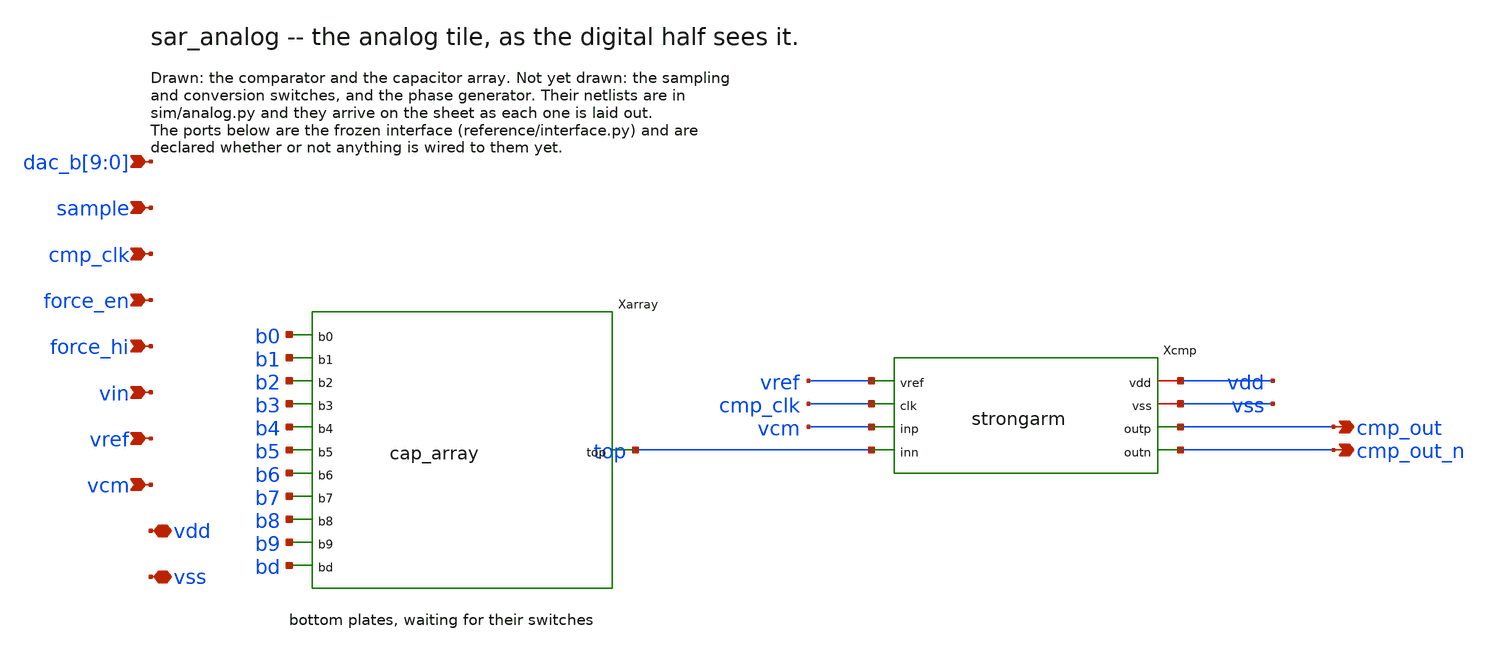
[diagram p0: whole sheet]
** sch_path: xschem/sar_analog.sch
**.subckt sar_analog
*+ dac_b[9],dac_b[8],dac_b[7],dac_b[6],dac_b[5],dac_b[4],dac_b[3],dac_b[2],dac_b[1],dac_b[0] sample cmp_clk force_en force_hi vin vref vcm vdd vss cmp_out cmp_out_n
*.ipin dac_b[9],dac_b[8],dac_b[7],dac_b[6],dac_b[5],dac_b[4],dac_b[3],dac_b[2],dac_b[1],dac_b[0]
*.ipin sample
*.ipin cmp_clk
*.ipin force_en
*.ipin force_hi
*.ipin vin
*.ipin vref
*.ipin vcm
*.iopin vdd
*.iopin vss
*.opin cmp_out
*.opin cmp_out_n
Xcmp vdd vss vref cmp_clk vcm top cmp_out cmp_out_n strongarm
Xarray top b0 b1 b2 b3 b4 b5 b6 b7 b8 b9 bd cap_array
**.ends

* expanding   symbol:  strongarm.sym # of pins=8
** sym_path: xschem/strongarm.sym
** sch_path: xschem/strongarm.sch
.subckt strongarm vdd vss vref clk inp inn outp outn
*.iopin vdd
*.iopin vss
*.ipin vref
*.ipin clk
*.ipin inp
*.ipin inn
*.opin outp
*.opin outn
Xinvp clk_i clk vdd vdd sky130_fd_pr__pfet_01v8 L=0.15 W=2 nf=1 ad='int((nf+1)/2) * W/nf * 0.29' as='int((nf+2)/2) * W/nf * 0.29'
+ pd='2*int((nf+1)/2) * (W/nf + 0.29)' ps='2*int((nf+2)/2) * (W/nf + 0.29)' nrd='0.29 / W' nrs='0.29 / W'
+ sa=0 sb=0 sd=0 mult=1 m=1
Xinvn clk_i clk vss vss sky130_fd_pr__nfet_01v8 L=0.15 W=2 nf=1 ad='int((1 + 1)/2) * 2 / 1 * 0.29' as='int((1 + 2)/2) * 2 / 1 * 0.29'
+ pd='2*int((1 + 1)/2) * (2 / 1 + 0.29)' ps='2*int((1 + 2)/2) * (2 / 1 + 0.29)' nrd='0.29 / 2 ' nrs='0.29 / 2 '
+ sa=0 sb=0 sd=0 mult=1 m=1
Xbref bias vref vss vss sky130_fd_pr__nfet_01v8 L=2 W=1 nf=1 ad='int((1 + 1)/2) * 1 / 1 * 0.29' as='int((1 + 2)/2) * 1 / 1 * 0.29'
+ pd='2*int((1 + 1)/2) * (1 / 1 + 0.29)' ps='2*int((1 + 2)/2) * (1 / 1 + 0.29)' nrd='0.29 / 1 ' nrs='0.29 / 1 '
+ sa=0 sb=0 sd=0 mult=1 m=1
Xbdio bias bias vdd vdd sky130_fd_pr__pfet_01v8 L=0.5 W=1 nf=1 ad='int((nf+1)/2) * W/nf * 0.29' as='int((nf+2)/2) * W/nf * 0.29'
+ pd='2*int((nf+1)/2) * (W/nf + 0.29)' ps='2*int((nf+2)/2) * (W/nf + 0.29)' nrd='0.29 / W' nrs='0.29 / W'
+ sa=0 sb=0 sd=0 mult=1 m=1
Xbgoff tgate clk vdd vdd sky130_fd_pr__pfet_01v8 L=0.15 W=1 nf=1 ad='int((nf+1)/2) * W/nf * 0.29' as='int((nf+2)/2) * W/nf * 0.29'
+ pd='2*int((nf+1)/2) * (W/nf + 0.29)' ps='2*int((nf+2)/2) * (W/nf + 0.29)' nrd='0.29 / W' nrs='0.29 / W'
+ sa=0 sb=0 sd=0 mult=1 m=1
Xbgon bias clk tgate vss sky130_fd_pr__nfet_01v8 L=0.15 W=1 nf=1 ad='int((1 + 1)/2) * 1 / 1 * 0.29' as='int((1 + 2)/2) * 1 / 1 * 0.29'
+ pd='2*int((1 + 1)/2) * (1 / 1 + 0.29)' ps='2*int((1 + 2)/2) * (1 / 1 + 0.29)' nrd='0.29 / 1 ' nrs='0.29 / 1 '
+ sa=0 sb=0 sd=0 mult=1 m=1
Cbias bias vss 1e-13 m=1
Xtail tail tgate vdd vdd sky130_fd_pr__pfet_01v8 L=0.5 W=2 nf=1 ad='int((nf+1)/2) * W/nf * 0.29' as='int((nf+2)/2) * W/nf * 0.29'
+ pd='2*int((nf+1)/2) * (W/nf + 0.29)' ps='2*int((nf+2)/2) * (W/nf + 0.29)' nrd='0.29 / W' nrs='0.29 / W'
+ sa=0 sb=0 sd=0 mult=1 m=1
Xinp xn inp tail vdd sky130_fd_pr__pfet_01v8 L=0.5 W=4 nf=1 ad='int((nf+1)/2) * W/nf * 0.29' as='int((nf+2)/2) * W/nf * 0.29'
+ pd='2*int((nf+1)/2) * (W/nf + 0.29)' ps='2*int((nf+2)/2) * (W/nf + 0.29)' nrd='0.29 / W' nrs='0.29 / W'
+ sa=0 sb=0 sd=0 mult=1 m=1
Xinn xp inn tail vdd sky130_fd_pr__pfet_01v8 L=0.5 W=4 nf=1 ad='int((nf+1)/2) * W/nf * 0.29' as='int((nf+2)/2) * W/nf * 0.29'
+ pd='2*int((nf+1)/2) * (W/nf + 0.29)' ps='2*int((nf+2)/2) * (W/nf + 0.29)' nrd='0.29 / W' nrs='0.29 / W'
+ sa=0 sb=0 sd=0 mult=1 m=1
Xlchp outp outn xp vdd sky130_fd_pr__pfet_01v8 L=0.15 W=1 nf=1 ad='int((nf+1)/2) * W/nf * 0.29' as='int((nf+2)/2) * W/nf * 0.29'
+ pd='2*int((nf+1)/2) * (W/nf + 0.29)' ps='2*int((nf+2)/2) * (W/nf + 0.29)' nrd='0.29 / W' nrs='0.29 / W'
+ sa=0 sb=0 sd=0 mult=1 m=1
Xlchn outn outp xn vdd sky130_fd_pr__pfet_01v8 L=0.15 W=1 nf=1 ad='int((nf+1)/2) * W/nf * 0.29' as='int((nf+2)/2) * W/nf * 0.29'
+ pd='2*int((nf+1)/2) * (W/nf + 0.29)' ps='2*int((nf+2)/2) * (W/nf + 0.29)' nrd='0.29 / W' nrs='0.29 / W'
+ sa=0 sb=0 sd=0 mult=1 m=1
Xldp outp outn vss vss sky130_fd_pr__nfet_01v8 L=0.15 W=2 nf=1 ad='int((1 + 1)/2) * 2 / 1 * 0.29' as='int((1 + 2)/2) * 2 / 1 * 0.29'
+ pd='2*int((1 + 1)/2) * (2 / 1 + 0.29)' ps='2*int((1 + 2)/2) * (2 / 1 + 0.29)' nrd='0.29 / 2 ' nrs='0.29 / 2 '
+ sa=0 sb=0 sd=0 mult=1 m=1
Xldn outn outp vss vss sky130_fd_pr__nfet_01v8 L=0.15 W=2 nf=1 ad='int((1 + 1)/2) * 2 / 1 * 0.29' as='int((1 + 2)/2) * 2 / 1 * 0.29'
+ pd='2*int((1 + 1)/2) * (2 / 1 + 0.29)' ps='2*int((1 + 2)/2) * (2 / 1 + 0.29)' nrd='0.29 / 2 ' nrs='0.29 / 2 '
+ sa=0 sb=0 sd=0 mult=1 m=1
Xprep outp clk_i vss vss sky130_fd_pr__nfet_01v8 L=0.15 W=2 nf=1 ad='int((1 + 1)/2) * 2 / 1 * 0.29' as='int((1 + 2)/2) * 2 / 1 * 0.29'
+ pd='2*int((1 + 1)/2) * (2 / 1 + 0.29)' ps='2*int((1 + 2)/2) * (2 / 1 + 0.29)' nrd='0.29 / 2 ' nrs='0.29 / 2 '
+ sa=0 sb=0 sd=0 mult=1 m=1
Xpren outn clk_i vss vss sky130_fd_pr__nfet_01v8 L=0.15 W=2 nf=1 ad='int((1 + 1)/2) * 2 / 1 * 0.29' as='int((1 + 2)/2) * 2 / 1 * 0.29'
+ pd='2*int((1 + 1)/2) * (2 / 1 + 0.29)' ps='2*int((1 + 2)/2) * (2 / 1 + 0.29)' nrd='0.29 / 2 ' nrs='0.29 / 2 '
+ sa=0 sb=0 sd=0 mult=1 m=1
Xprxp xp clk_i vss vss sky130_fd_pr__nfet_01v8 L=0.15 W=2 nf=1 ad='int((1 + 1)/2) * 2 / 1 * 0.29' as='int((1 + 2)/2) * 2 / 1 * 0.29'
+ pd='2*int((1 + 1)/2) * (2 / 1 + 0.29)' ps='2*int((1 + 2)/2) * (2 / 1 + 0.29)' nrd='0.29 / 2 ' nrs='0.29 / 2 '
+ sa=0 sb=0 sd=0 mult=1 m=1
Xprxn xn clk_i vss vss sky130_fd_pr__nfet_01v8 L=0.15 W=2 nf=1 ad='int((1 + 1)/2) * 2 / 1 * 0.29' as='int((1 + 2)/2) * 2 / 1 * 0.29'
+ pd='2*int((1 + 1)/2) * (2 / 1 + 0.29)' ps='2*int((1 + 2)/2) * (2 / 1 + 0.29)' nrd='0.29 / 2 ' nrs='0.29 / 2 '
+ sa=0 sb=0 sd=0 mult=1 m=1
Cxp xp vss 2e-13 m=1
Cxn xn vss 2e-13 m=1
Coutp outp vss 1e-14 m=1
Coutn outn vss 1e-14 m=1
.ends


* expanding   symbol:  cap_array.sym # of pins=12
** sym_path: xschem/cap_array.sym
** sch_path: xschem/cap_array.sch
.subckt cap_array top b0 b1 b2 b3 b4 b5 b6 b7 b8 b9 bd
*.iopin top
*.iopin b0
*.iopin b1
*.iopin b2
*.iopin b3
*.iopin b4
*.iopin b5
*.iopin b6
*.iopin b7
*.iopin b8
*.iopin b9
*.iopin bd
Xu0 top b0 sky130_fd_pr__cap_mim_m3_1 w=2 l=2 mult=1 m=1
Xu1 top b1 sky130_fd_pr__cap_mim_m3_1 w=2 l=2 mult=2 m=2
Xu2 top b2 sky130_fd_pr__cap_mim_m3_1 w=2 l=2 mult=4 m=4
Xu3 top b3 sky130_fd_pr__cap_mim_m3_1 w=2 l=2 mult=8 m=8
Xu4 top b4 sky130_fd_pr__cap_mim_m3_1 w=2 l=2 mult=16 m=16
Xu5 top b5 sky130_fd_pr__cap_mim_m3_1 w=2 l=2 mult=32 m=32
Xu6 top b6 sky130_fd_pr__cap_mim_m3_1 w=2 l=2 mult=64 m=64
Xu7 top b7 sky130_fd_pr__cap_mim_m3_1 w=2 l=2 mult=128 m=128
Xu8 top b8 sky130_fd_pr__cap_mim_m3_1 w=2 l=2 mult=256 m=256
Xu9 top b9 sky130_fd_pr__cap_mim_m3_1 w=2 l=2 mult=512 m=512
Xud top bd sky130_fd_pr__cap_mim_m3_1 w=2 l=2 mult=1 m=1
.ends

.end
